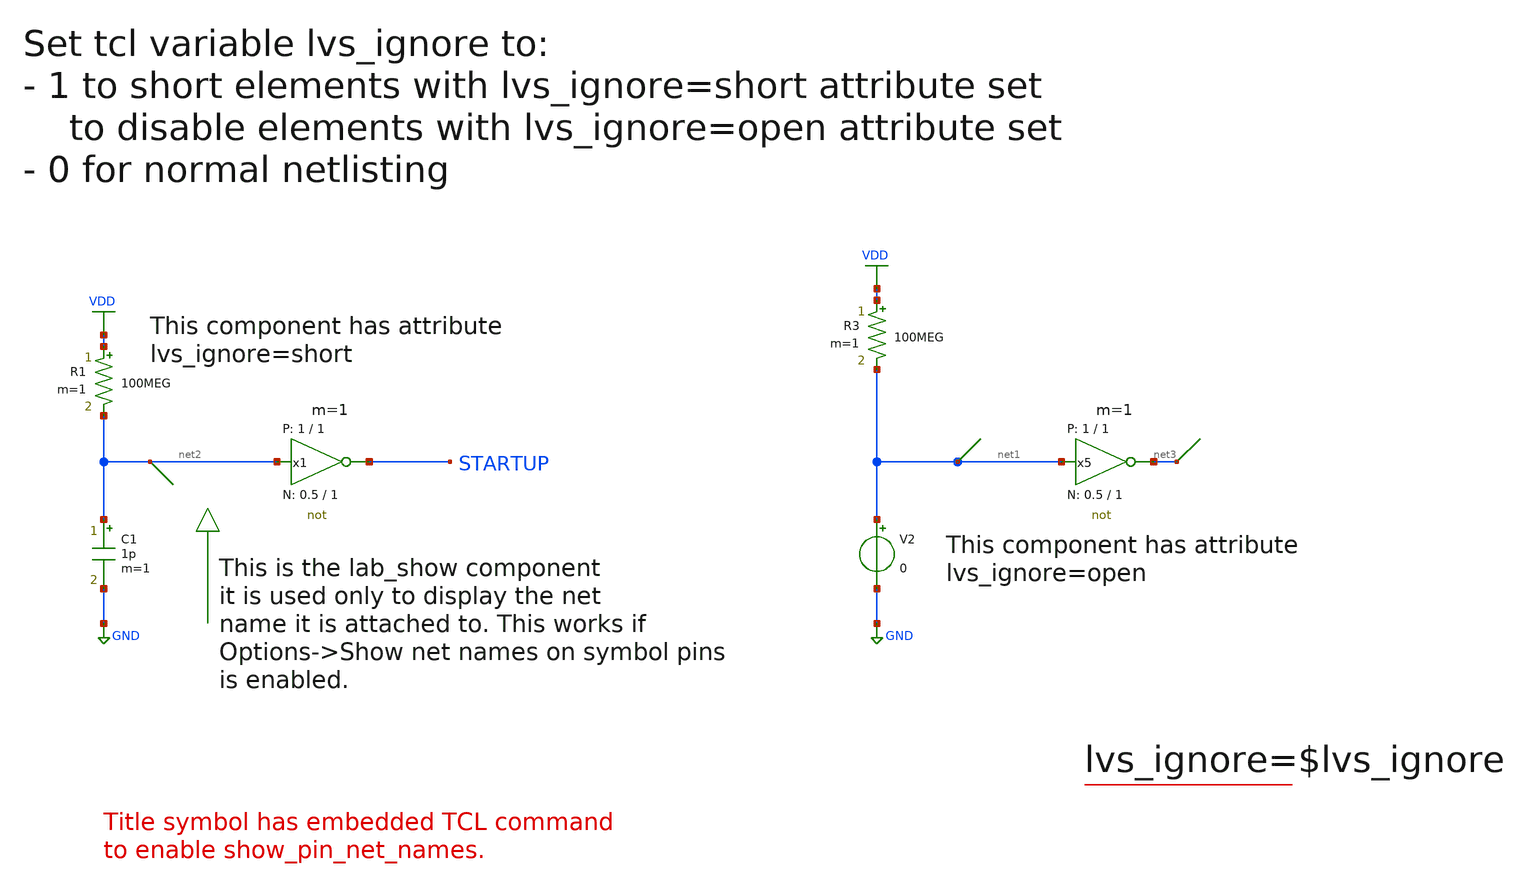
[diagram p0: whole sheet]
** sch_path: sky130A/xschem_libs/sky130_tests/test_lvs_ignore/schematic/test_lvs_ignore.sch
* Copyright 2021 Stefan Frederik Schippers
* Licensed under the Apache License, Version 2.0 (the "License");
* you may not use this file except in compliance with the License.
* You may obtain a copy of the License at
* https://www.apache.org/licenses/LICENSE-2.0
* Unless required by applicable law or agreed to in writing, software
* distributed under the License is distributed on an "AS IS" BASIS,
* WITHOUT WARRANTIES OR CONDITIONS OF ANY KIND, either express or implied.
* See the License for the specific language governing permissions and
* limitations under the License.
**.subckt test_lvs_ignore
x5 net3 net1 VCC VSS not W_N=0.5 L_N=1 W_P=1 L_P=1 m=1
V2 net1 GND 0
R1 VDD net2 100MEG m=1
C1 net2 GND 1p m=1
R3 VDD net1 100MEG m=1
x1 STARTUP net2 VCC VSS not W_N=0.5 L_N=1 W_P=1 L_P=1 m=1
**.ends

* expanding   symbol:  sky130_tests/not.sym # of pins=2
** sym_path: sky130_tests/not.sym
** sch_path: sky130_tests/not.sch
.subckt not y a VCCPIN VSSPIN     W_N=1 L_N=0.15 W_P=2 L_P=0.15
*.opin y
*.ipin a
XM1 DN a VSSPIN VSSPIN sky130_fd_pr__nfet_01v8 L=L_N W=W_N nf=1 ad='int((1 + 1)/2) * W_N / 1 * 0.29'
+ as='int((1 + 2)/2) * W_N / 1 * 0.29' pd='2*int((1 + 1)/2) * (W_N / 1 + 0.29)' ps='2*int((1 + 2)/2) * (W_N / 1 + 0.29)'
+ nrd='0.29 / W_N ' nrs='0.29 / W_N ' sa=0 sb=0 sd=0 mult=1 m=1
XM2 DP a VCCPIN VCCPIN sky130_fd_pr__pfet_01v8 L=L_P W=W_P nf=1 ad='int((nf+1)/2) * W/nf * 0.29' as='int((nf+2)/2) * W/nf * 0.29'
+ pd='2*int((nf+1)/2) * (W/nf + 0.29)' ps='2*int((nf+2)/2) * (W/nf + 0.29)' nrd='0.29 / W' nrs='0.29 / W'
+ sa=0 sb=0 sd=0 mult=1 m=1
Vmeas DP y 0
.save i(vmeas)
Vmeas1 y DN 0
.save i(vmeas1)
.save v(dp)
.save v(dn)
.ends

.GLOBAL GND
.GLOBAL VDD
.end
